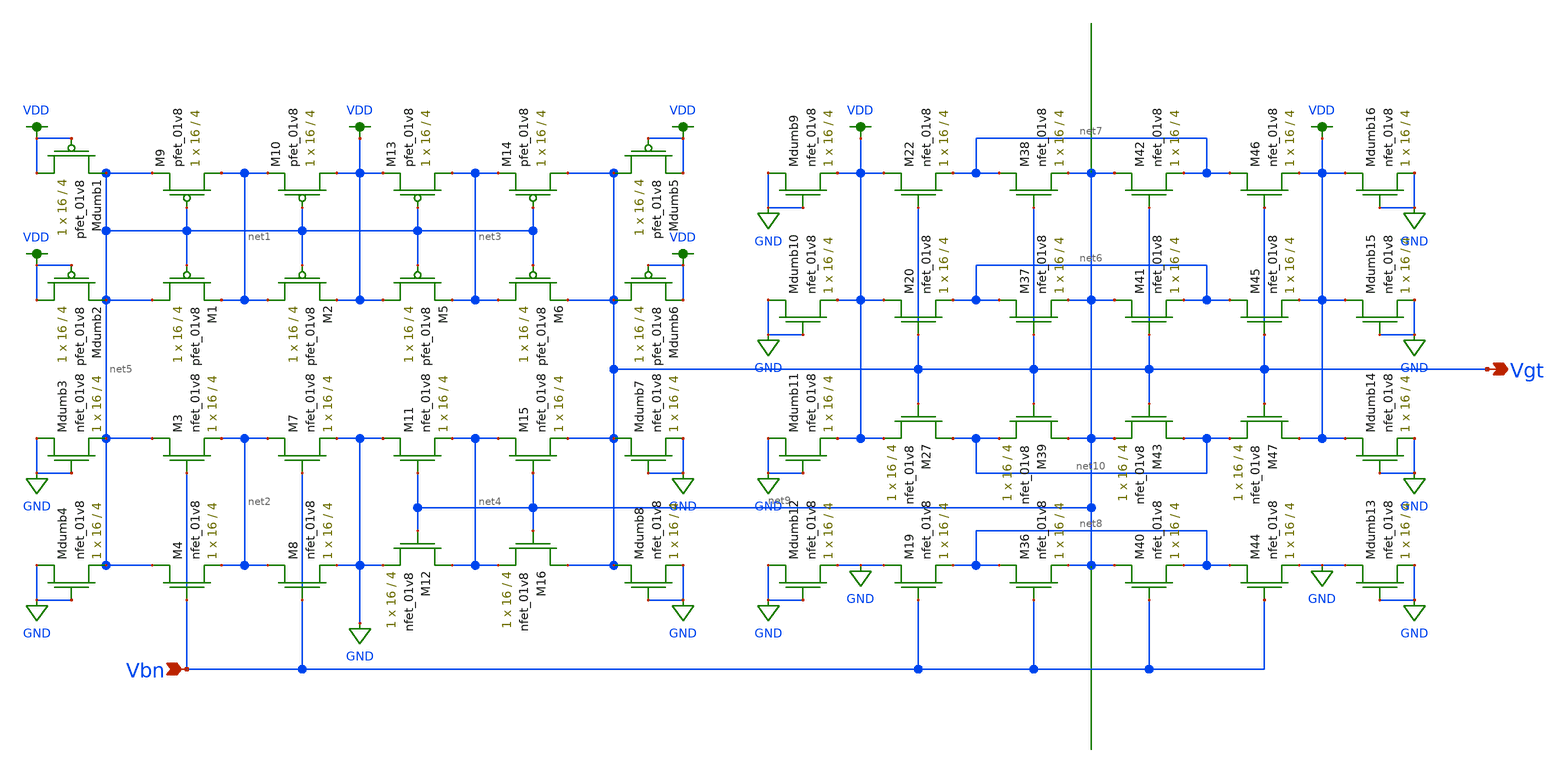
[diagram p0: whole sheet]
** sch_path: schematic/LDS/Vg_gen_lvs.sch
**.subckt Vg_gen_lvs Vbn Vgt
*.ipin Vbn
*.opin Vgt
XM1 net5 net5 net1 VDD sky130_fd_pr__pfet_01v8 L=4 W=16 nf=1 ad='int((nf+1)/2) * W/nf * 0.29' as='int((nf+2)/2) * W/nf * 0.29'
+ pd='2*int((nf+1)/2) * (W/nf + 0.29)' ps='2*int((nf+2)/2) * (W/nf + 0.29)' nrd='0.29 / W' nrs='0.29 / W'
+ sa=0 sb=0 sd=0 mult=1 m=1
XM2 net1 net5 VDD VDD sky130_fd_pr__pfet_01v8 L=4 W=16 nf=1 ad='int((nf+1)/2) * W/nf * 0.29' as='int((nf+2)/2) * W/nf * 0.29'
+ pd='2*int((nf+1)/2) * (W/nf + 0.29)' ps='2*int((nf+2)/2) * (W/nf + 0.29)' nrd='0.29 / W' nrs='0.29 / W'
+ sa=0 sb=0 sd=0 mult=1 m=1
XM5 VDD net5 net3 VDD sky130_fd_pr__pfet_01v8 L=4 W=16 nf=1 ad='int((nf+1)/2) * W/nf * 0.29' as='int((nf+2)/2) * W/nf * 0.29'
+ pd='2*int((nf+1)/2) * (W/nf + 0.29)' ps='2*int((nf+2)/2) * (W/nf + 0.29)' nrd='0.29 / W' nrs='0.29 / W'
+ sa=0 sb=0 sd=0 mult=1 m=1
XM6 net3 net5 Vgt VDD sky130_fd_pr__pfet_01v8 L=4 W=16 nf=1 ad='int((nf+1)/2) * W/nf * 0.29' as='int((nf+2)/2) * W/nf * 0.29'
+ pd='2*int((nf+1)/2) * (W/nf + 0.29)' ps='2*int((nf+2)/2) * (W/nf + 0.29)' nrd='0.29 / W' nrs='0.29 / W'
+ sa=0 sb=0 sd=0 mult=1 m=1
XM9 net1 net5 net5 VDD sky130_fd_pr__pfet_01v8 L=4 W=16 nf=1 ad='int((nf+1)/2) * W/nf * 0.29' as='int((nf+2)/2) * W/nf * 0.29'
+ pd='2*int((nf+1)/2) * (W/nf + 0.29)' ps='2*int((nf+2)/2) * (W/nf + 0.29)' nrd='0.29 / W' nrs='0.29 / W'
+ sa=0 sb=0 sd=0 mult=1 m=1
XM10 VDD net5 net1 VDD sky130_fd_pr__pfet_01v8 L=4 W=16 nf=1 ad='int((nf+1)/2) * W/nf * 0.29' as='int((nf+2)/2) * W/nf * 0.29'
+ pd='2*int((nf+1)/2) * (W/nf + 0.29)' ps='2*int((nf+2)/2) * (W/nf + 0.29)' nrd='0.29 / W' nrs='0.29 / W'
+ sa=0 sb=0 sd=0 mult=1 m=1
XM13 net3 net5 VDD VDD sky130_fd_pr__pfet_01v8 L=4 W=16 nf=1 ad='int((nf+1)/2) * W/nf * 0.29' as='int((nf+2)/2) * W/nf * 0.29'
+ pd='2*int((nf+1)/2) * (W/nf + 0.29)' ps='2*int((nf+2)/2) * (W/nf + 0.29)' nrd='0.29 / W' nrs='0.29 / W'
+ sa=0 sb=0 sd=0 mult=1 m=1
XM14 Vgt net5 net3 VDD sky130_fd_pr__pfet_01v8 L=4 W=16 nf=1 ad='int((nf+1)/2) * W/nf * 0.29' as='int((nf+2)/2) * W/nf * 0.29'
+ pd='2*int((nf+1)/2) * (W/nf + 0.29)' ps='2*int((nf+2)/2) * (W/nf + 0.29)' nrd='0.29 / W' nrs='0.29 / W'
+ sa=0 sb=0 sd=0 mult=1 m=1
XMdumb2 VDD VDD net5 VDD sky130_fd_pr__pfet_01v8 L=4 W=16 nf=1 ad='int((nf+1)/2) * W/nf * 0.29' as='int((nf+2)/2) * W/nf * 0.29'
+ pd='2*int((nf+1)/2) * (W/nf + 0.29)' ps='2*int((nf+2)/2) * (W/nf + 0.29)' nrd='0.29 / W' nrs='0.29 / W'
+ sa=0 sb=0 sd=0 mult=1 m=1
XMdumb1 VDD VDD net5 VDD sky130_fd_pr__pfet_01v8 L=4 W=16 nf=1 ad='int((nf+1)/2) * W/nf * 0.29' as='int((nf+2)/2) * W/nf * 0.29'
+ pd='2*int((nf+1)/2) * (W/nf + 0.29)' ps='2*int((nf+2)/2) * (W/nf + 0.29)' nrd='0.29 / W' nrs='0.29 / W'
+ sa=0 sb=0 sd=0 mult=1 m=1
XMdumb6 Vgt VDD VDD VDD sky130_fd_pr__pfet_01v8 L=4 W=16 nf=1 ad='int((nf+1)/2) * W/nf * 0.29' as='int((nf+2)/2) * W/nf * 0.29'
+ pd='2*int((nf+1)/2) * (W/nf + 0.29)' ps='2*int((nf+2)/2) * (W/nf + 0.29)' nrd='0.29 / W' nrs='0.29 / W'
+ sa=0 sb=0 sd=0 mult=1 m=1
XMdumb5 Vgt VDD VDD VDD sky130_fd_pr__pfet_01v8 L=4 W=16 nf=1 ad='int((nf+1)/2) * W/nf * 0.29' as='int((nf+2)/2) * W/nf * 0.29'
+ pd='2*int((nf+1)/2) * (W/nf + 0.29)' ps='2*int((nf+2)/2) * (W/nf + 0.29)' nrd='0.29 / W' nrs='0.29 / W'
+ sa=0 sb=0 sd=0 mult=1 m=1
XMdumb3 GND GND net5 GND sky130_fd_pr__nfet_01v8 L=4 W=16 nf=1 ad='int((nf+1)/2) * W/nf * 0.29' as='int((nf+2)/2) * W/nf * 0.29'
+ pd='2*int((nf+1)/2) * (W/nf + 0.29)' ps='2*int((nf+2)/2) * (W/nf + 0.29)' nrd='0.29 / W' nrs='0.29 / W'
+ sa=0 sb=0 sd=0 mult=1 m=1
XMdumb4 GND GND net5 GND sky130_fd_pr__nfet_01v8 L=4 W=16 nf=1 ad='int((nf+1)/2) * W/nf * 0.29' as='int((nf+2)/2) * W/nf * 0.29'
+ pd='2*int((nf+1)/2) * (W/nf + 0.29)' ps='2*int((nf+2)/2) * (W/nf + 0.29)' nrd='0.29 / W' nrs='0.29 / W'
+ sa=0 sb=0 sd=0 mult=1 m=1
XM3 net5 Vbn net2 GND sky130_fd_pr__nfet_01v8 L=4 W=16 nf=1 ad='int((nf+1)/2) * W/nf * 0.29' as='int((nf+2)/2) * W/nf * 0.29'
+ pd='2*int((nf+1)/2) * (W/nf + 0.29)' ps='2*int((nf+2)/2) * (W/nf + 0.29)' nrd='0.29 / W' nrs='0.29 / W'
+ sa=0 sb=0 sd=0 mult=1 m=1
XM4 net5 Vbn net2 GND sky130_fd_pr__nfet_01v8 L=4 W=16 nf=1 ad='int((nf+1)/2) * W/nf * 0.29' as='int((nf+2)/2) * W/nf * 0.29'
+ pd='2*int((nf+1)/2) * (W/nf + 0.29)' ps='2*int((nf+2)/2) * (W/nf + 0.29)' nrd='0.29 / W' nrs='0.29 / W'
+ sa=0 sb=0 sd=0 mult=1 m=1
XM7 net2 Vbn GND GND sky130_fd_pr__nfet_01v8 L=4 W=16 nf=1 ad='int((nf+1)/2) * W/nf * 0.29' as='int((nf+2)/2) * W/nf * 0.29'
+ pd='2*int((nf+1)/2) * (W/nf + 0.29)' ps='2*int((nf+2)/2) * (W/nf + 0.29)' nrd='0.29 / W' nrs='0.29 / W'
+ sa=0 sb=0 sd=0 mult=1 m=1
XM8 net2 Vbn GND GND sky130_fd_pr__nfet_01v8 L=4 W=16 nf=1 ad='int((nf+1)/2) * W/nf * 0.29' as='int((nf+2)/2) * W/nf * 0.29'
+ pd='2*int((nf+1)/2) * (W/nf + 0.29)' ps='2*int((nf+2)/2) * (W/nf + 0.29)' nrd='0.29 / W' nrs='0.29 / W'
+ sa=0 sb=0 sd=0 mult=1 m=1
XM11 GND net9 net4 GND sky130_fd_pr__nfet_01v8 L=4 W=16 nf=1 ad='int((nf+1)/2) * W/nf * 0.29' as='int((nf+2)/2) * W/nf * 0.29'
+ pd='2*int((nf+1)/2) * (W/nf + 0.29)' ps='2*int((nf+2)/2) * (W/nf + 0.29)' nrd='0.29 / W' nrs='0.29 / W'
+ sa=0 sb=0 sd=0 mult=1 m=1
XM12 net4 net9 GND GND sky130_fd_pr__nfet_01v8 L=4 W=16 nf=1 ad='int((nf+1)/2) * W/nf * 0.29' as='int((nf+2)/2) * W/nf * 0.29'
+ pd='2*int((nf+1)/2) * (W/nf + 0.29)' ps='2*int((nf+2)/2) * (W/nf + 0.29)' nrd='0.29 / W' nrs='0.29 / W'
+ sa=0 sb=0 sd=0 mult=1 m=1
XM15 net4 net9 Vgt GND sky130_fd_pr__nfet_01v8 L=4 W=16 nf=1 ad='int((nf+1)/2) * W/nf * 0.29' as='int((nf+2)/2) * W/nf * 0.29'
+ pd='2*int((nf+1)/2) * (W/nf + 0.29)' ps='2*int((nf+2)/2) * (W/nf + 0.29)' nrd='0.29 / W' nrs='0.29 / W'
+ sa=0 sb=0 sd=0 mult=1 m=1
XM16 Vgt net9 net4 GND sky130_fd_pr__nfet_01v8 L=4 W=16 nf=1 ad='int((nf+1)/2) * W/nf * 0.29' as='int((nf+2)/2) * W/nf * 0.29'
+ pd='2*int((nf+1)/2) * (W/nf + 0.29)' ps='2*int((nf+2)/2) * (W/nf + 0.29)' nrd='0.29 / W' nrs='0.29 / W'
+ sa=0 sb=0 sd=0 mult=1 m=1
XMdumb7 Vgt GND GND GND sky130_fd_pr__nfet_01v8 L=4 W=16 nf=1 ad='int((nf+1)/2) * W/nf * 0.29' as='int((nf+2)/2) * W/nf * 0.29'
+ pd='2*int((nf+1)/2) * (W/nf + 0.29)' ps='2*int((nf+2)/2) * (W/nf + 0.29)' nrd='0.29 / W' nrs='0.29 / W'
+ sa=0 sb=0 sd=0 mult=1 m=1
XMdumb8 Vgt GND GND GND sky130_fd_pr__nfet_01v8 L=4 W=16 nf=1 ad='int((nf+1)/2) * W/nf * 0.29' as='int((nf+2)/2) * W/nf * 0.29'
+ pd='2*int((nf+1)/2) * (W/nf + 0.29)' ps='2*int((nf+2)/2) * (W/nf + 0.29)' nrd='0.29 / W' nrs='0.29 / W'
+ sa=0 sb=0 sd=0 mult=1 m=1
XM19 GND Vbn net8 GND sky130_fd_pr__nfet_01v8 L=4 W=16 nf=1 ad='int((nf+1)/2) * W/nf * 0.29' as='int((nf+2)/2) * W/nf * 0.29'
+ pd='2*int((nf+1)/2) * (W/nf + 0.29)' ps='2*int((nf+2)/2) * (W/nf + 0.29)' nrd='0.29 / W' nrs='0.29 / W'
+ sa=0 sb=0 sd=0 mult=1 m=1
XM20 VDD Vgt net6 GND sky130_fd_pr__nfet_01v8 L=4 W=16 nf=1 ad='int((nf+1)/2) * W/nf * 0.29' as='int((nf+2)/2) * W/nf * 0.29'
+ pd='2*int((nf+1)/2) * (W/nf + 0.29)' ps='2*int((nf+2)/2) * (W/nf + 0.29)' nrd='0.29 / W' nrs='0.29 / W'
+ sa=0 sb=0 sd=0 mult=1 m=1
XM22 VDD Vgt net7 GND sky130_fd_pr__nfet_01v8 L=4 W=16 nf=1 ad='int((nf+1)/2) * W/nf * 0.29' as='int((nf+2)/2) * W/nf * 0.29'
+ pd='2*int((nf+1)/2) * (W/nf + 0.29)' ps='2*int((nf+2)/2) * (W/nf + 0.29)' nrd='0.29 / W' nrs='0.29 / W'
+ sa=0 sb=0 sd=0 mult=1 m=1
XM27 net10 Vgt VDD GND sky130_fd_pr__nfet_01v8 L=4 W=16 nf=1 ad='int((nf+1)/2) * W/nf * 0.29' as='int((nf+2)/2) * W/nf * 0.29'
+ pd='2*int((nf+1)/2) * (W/nf + 0.29)' ps='2*int((nf+2)/2) * (W/nf + 0.29)' nrd='0.29 / W' nrs='0.29 / W'
+ sa=0 sb=0 sd=0 mult=1 m=1
XMdumb13 GND GND GND GND sky130_fd_pr__nfet_01v8 L=4 W=16 nf=1 ad='int((nf+1)/2) * W/nf * 0.29' as='int((nf+2)/2) * W/nf * 0.29'
+ pd='2*int((nf+1)/2) * (W/nf + 0.29)' ps='2*int((nf+2)/2) * (W/nf + 0.29)' nrd='0.29 / W' nrs='0.29 / W'
+ sa=0 sb=0 sd=0 mult=1 m=1
XMdumb15 VDD GND GND GND sky130_fd_pr__nfet_01v8 L=4 W=16 nf=1 ad='int((nf+1)/2) * W/nf * 0.29' as='int((nf+2)/2) * W/nf * 0.29'
+ pd='2*int((nf+1)/2) * (W/nf + 0.29)' ps='2*int((nf+2)/2) * (W/nf + 0.29)' nrd='0.29 / W' nrs='0.29 / W'
+ sa=0 sb=0 sd=0 mult=1 m=1
XMdumb16 VDD GND GND GND sky130_fd_pr__nfet_01v8 L=4 W=16 nf=1 ad='int((nf+1)/2) * W/nf * 0.29' as='int((nf+2)/2) * W/nf * 0.29'
+ pd='2*int((nf+1)/2) * (W/nf + 0.29)' ps='2*int((nf+2)/2) * (W/nf + 0.29)' nrd='0.29 / W' nrs='0.29 / W'
+ sa=0 sb=0 sd=0 mult=1 m=1
XMdumb14 VDD GND GND GND sky130_fd_pr__nfet_01v8 L=4 W=16 nf=1 ad='int((nf+1)/2) * W/nf * 0.29' as='int((nf+2)/2) * W/nf * 0.29'
+ pd='2*int((nf+1)/2) * (W/nf + 0.29)' ps='2*int((nf+2)/2) * (W/nf + 0.29)' nrd='0.29 / W' nrs='0.29 / W'
+ sa=0 sb=0 sd=0 mult=1 m=1
XMdumb12 GND GND GND GND sky130_fd_pr__nfet_01v8 L=4 W=16 nf=1 ad='int((nf+1)/2) * W/nf * 0.29' as='int((nf+2)/2) * W/nf * 0.29'
+ pd='2*int((nf+1)/2) * (W/nf + 0.29)' ps='2*int((nf+2)/2) * (W/nf + 0.29)' nrd='0.29 / W' nrs='0.29 / W'
+ sa=0 sb=0 sd=0 mult=1 m=1
XMdumb10 GND GND VDD GND sky130_fd_pr__nfet_01v8 L=4 W=16 nf=1 ad='int((nf+1)/2) * W/nf * 0.29' as='int((nf+2)/2) * W/nf * 0.29'
+ pd='2*int((nf+1)/2) * (W/nf + 0.29)' ps='2*int((nf+2)/2) * (W/nf + 0.29)' nrd='0.29 / W' nrs='0.29 / W'
+ sa=0 sb=0 sd=0 mult=1 m=1
XMdumb9 GND GND VDD GND sky130_fd_pr__nfet_01v8 L=4 W=16 nf=1 ad='int((nf+1)/2) * W/nf * 0.29' as='int((nf+2)/2) * W/nf * 0.29'
+ pd='2*int((nf+1)/2) * (W/nf + 0.29)' ps='2*int((nf+2)/2) * (W/nf + 0.29)' nrd='0.29 / W' nrs='0.29 / W'
+ sa=0 sb=0 sd=0 mult=1 m=1
XMdumb11 GND GND VDD GND sky130_fd_pr__nfet_01v8 L=4 W=16 nf=1 ad='int((nf+1)/2) * W/nf * 0.29' as='int((nf+2)/2) * W/nf * 0.29'
+ pd='2*int((nf+1)/2) * (W/nf + 0.29)' ps='2*int((nf+2)/2) * (W/nf + 0.29)' nrd='0.29 / W' nrs='0.29 / W'
+ sa=0 sb=0 sd=0 mult=1 m=1
XM36 net8 Vbn net9 GND sky130_fd_pr__nfet_01v8 L=4 W=16 nf=1 ad='int((nf+1)/2) * W/nf * 0.29' as='int((nf+2)/2) * W/nf * 0.29'
+ pd='2*int((nf+1)/2) * (W/nf + 0.29)' ps='2*int((nf+2)/2) * (W/nf + 0.29)' nrd='0.29 / W' nrs='0.29 / W'
+ sa=0 sb=0 sd=0 mult=1 m=1
XM37 net6 Vgt net9 GND sky130_fd_pr__nfet_01v8 L=4 W=16 nf=1 ad='int((nf+1)/2) * W/nf * 0.29' as='int((nf+2)/2) * W/nf * 0.29'
+ pd='2*int((nf+1)/2) * (W/nf + 0.29)' ps='2*int((nf+2)/2) * (W/nf + 0.29)' nrd='0.29 / W' nrs='0.29 / W'
+ sa=0 sb=0 sd=0 mult=1 m=1
XM38 net7 Vgt net9 GND sky130_fd_pr__nfet_01v8 L=4 W=16 nf=1 ad='int((nf+1)/2) * W/nf * 0.29' as='int((nf+2)/2) * W/nf * 0.29'
+ pd='2*int((nf+1)/2) * (W/nf + 0.29)' ps='2*int((nf+2)/2) * (W/nf + 0.29)' nrd='0.29 / W' nrs='0.29 / W'
+ sa=0 sb=0 sd=0 mult=1 m=1
XM39 net9 Vgt net10 GND sky130_fd_pr__nfet_01v8 L=4 W=16 nf=1 ad='int((nf+1)/2) * W/nf * 0.29' as='int((nf+2)/2) * W/nf * 0.29'
+ pd='2*int((nf+1)/2) * (W/nf + 0.29)' ps='2*int((nf+2)/2) * (W/nf + 0.29)' nrd='0.29 / W' nrs='0.29 / W'
+ sa=0 sb=0 sd=0 mult=1 m=1
XM40 net9 Vbn net8 GND sky130_fd_pr__nfet_01v8 L=4 W=16 nf=1 ad='int((nf+1)/2) * W/nf * 0.29' as='int((nf+2)/2) * W/nf * 0.29'
+ pd='2*int((nf+1)/2) * (W/nf + 0.29)' ps='2*int((nf+2)/2) * (W/nf + 0.29)' nrd='0.29 / W' nrs='0.29 / W'
+ sa=0 sb=0 sd=0 mult=1 m=1
XM41 net9 Vgt net6 GND sky130_fd_pr__nfet_01v8 L=4 W=16 nf=1 ad='int((nf+1)/2) * W/nf * 0.29' as='int((nf+2)/2) * W/nf * 0.29'
+ pd='2*int((nf+1)/2) * (W/nf + 0.29)' ps='2*int((nf+2)/2) * (W/nf + 0.29)' nrd='0.29 / W' nrs='0.29 / W'
+ sa=0 sb=0 sd=0 mult=1 m=1
XM42 net9 Vgt net7 GND sky130_fd_pr__nfet_01v8 L=4 W=16 nf=1 ad='int((nf+1)/2) * W/nf * 0.29' as='int((nf+2)/2) * W/nf * 0.29'
+ pd='2*int((nf+1)/2) * (W/nf + 0.29)' ps='2*int((nf+2)/2) * (W/nf + 0.29)' nrd='0.29 / W' nrs='0.29 / W'
+ sa=0 sb=0 sd=0 mult=1 m=1
XM43 net10 Vgt net9 GND sky130_fd_pr__nfet_01v8 L=4 W=16 nf=1 ad='int((nf+1)/2) * W/nf * 0.29' as='int((nf+2)/2) * W/nf * 0.29'
+ pd='2*int((nf+1)/2) * (W/nf + 0.29)' ps='2*int((nf+2)/2) * (W/nf + 0.29)' nrd='0.29 / W' nrs='0.29 / W'
+ sa=0 sb=0 sd=0 mult=1 m=1
XM44 net8 Vbn GND GND sky130_fd_pr__nfet_01v8 L=4 W=16 nf=1 ad='int((nf+1)/2) * W/nf * 0.29' as='int((nf+2)/2) * W/nf * 0.29'
+ pd='2*int((nf+1)/2) * (W/nf + 0.29)' ps='2*int((nf+2)/2) * (W/nf + 0.29)' nrd='0.29 / W' nrs='0.29 / W'
+ sa=0 sb=0 sd=0 mult=1 m=1
XM45 net6 Vgt VDD GND sky130_fd_pr__nfet_01v8 L=4 W=16 nf=1 ad='int((nf+1)/2) * W/nf * 0.29' as='int((nf+2)/2) * W/nf * 0.29'
+ pd='2*int((nf+1)/2) * (W/nf + 0.29)' ps='2*int((nf+2)/2) * (W/nf + 0.29)' nrd='0.29 / W' nrs='0.29 / W'
+ sa=0 sb=0 sd=0 mult=1 m=1
XM46 net7 Vgt VDD GND sky130_fd_pr__nfet_01v8 L=4 W=16 nf=1 ad='int((nf+1)/2) * W/nf * 0.29' as='int((nf+2)/2) * W/nf * 0.29'
+ pd='2*int((nf+1)/2) * (W/nf + 0.29)' ps='2*int((nf+2)/2) * (W/nf + 0.29)' nrd='0.29 / W' nrs='0.29 / W'
+ sa=0 sb=0 sd=0 mult=1 m=1
XM47 VDD Vgt net10 GND sky130_fd_pr__nfet_01v8 L=4 W=16 nf=1 ad='int((nf+1)/2) * W/nf * 0.29' as='int((nf+2)/2) * W/nf * 0.29'
+ pd='2*int((nf+1)/2) * (W/nf + 0.29)' ps='2*int((nf+2)/2) * (W/nf + 0.29)' nrd='0.29 / W' nrs='0.29 / W'
+ sa=0 sb=0 sd=0 mult=1 m=1
**.ends
.GLOBAL GND
.GLOBAL VDD
.end
